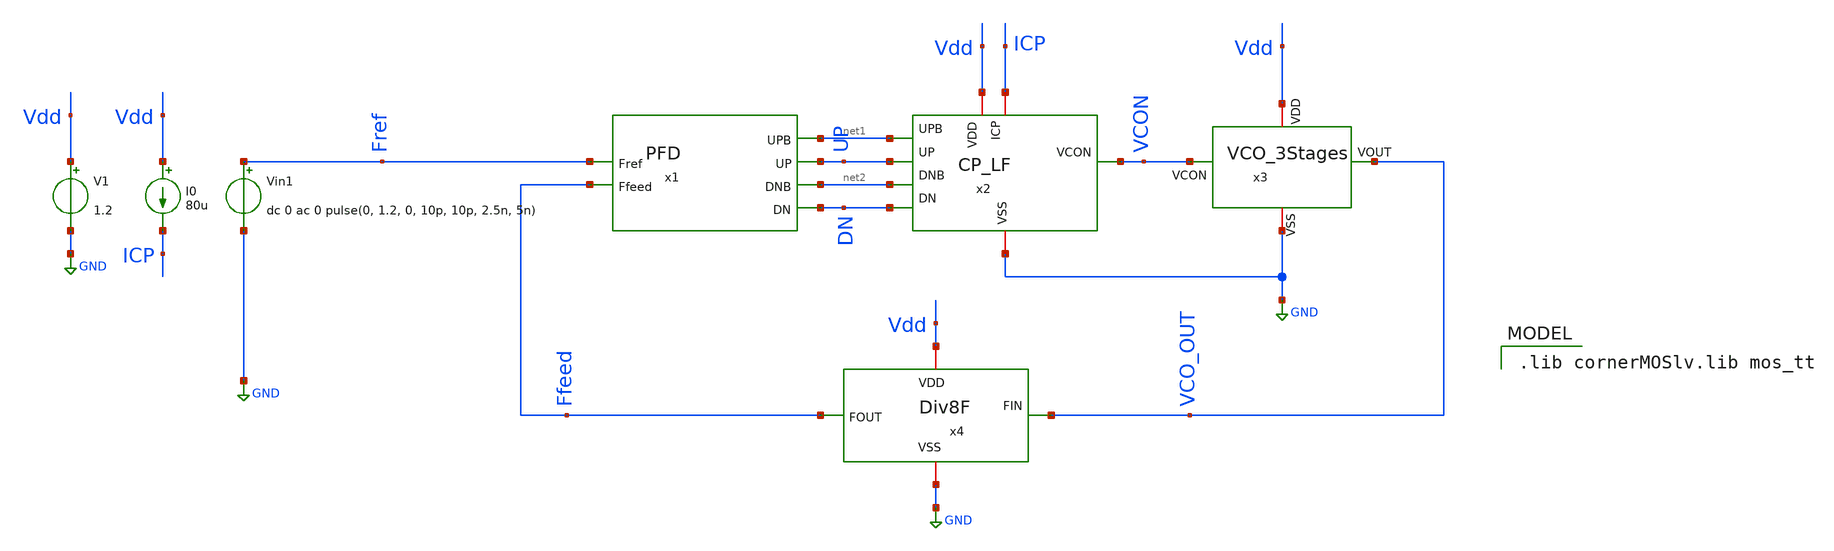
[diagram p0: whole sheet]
** sch_path: Team 1 Design/design_data/xschem/PLL_Completed/PLL_Completed_tb.sch
**.subckt PLL_Completed_tb
x1 Fref UP net1 DN net2 Ffeed PFD
x2 Vdd ICP GND net1 UP VCON net2 DN CP_LF
x3 Vdd VCO_OUT VCON GND VCO_3Stages
x4 Vdd Ffeed VCO_OUT GND Div8F
V1 Vdd GND 1.2
I0 Vdd ICP 80u
Vin1 Fref GND dc 0 ac 0 pulse(0, 1.2, 0, 10p, 10p, 2.5n, 5n)
**** begin user architecture code


.param temp=27
.control
save all
.options maxstep=10n reltol=1e-3 abstol=1e-6
tran 50p 600n
plot v(Fref)+10 v(Ffeed)+8 v(UP)+6 v(DN)+4 v(VCO_OUT)+2 v(VCON) xlimit 400n 600n
fft v(VCO_OUT)
plot db(mag(v(VCO_OUT))) xlabel 'Frequency (Hz)' xlimi 0 2Gig
.endc


 .lib cornerMOSlv.lib mos_tt

**** end user architecture code
**.ends
.GLOBAL GND
.end
